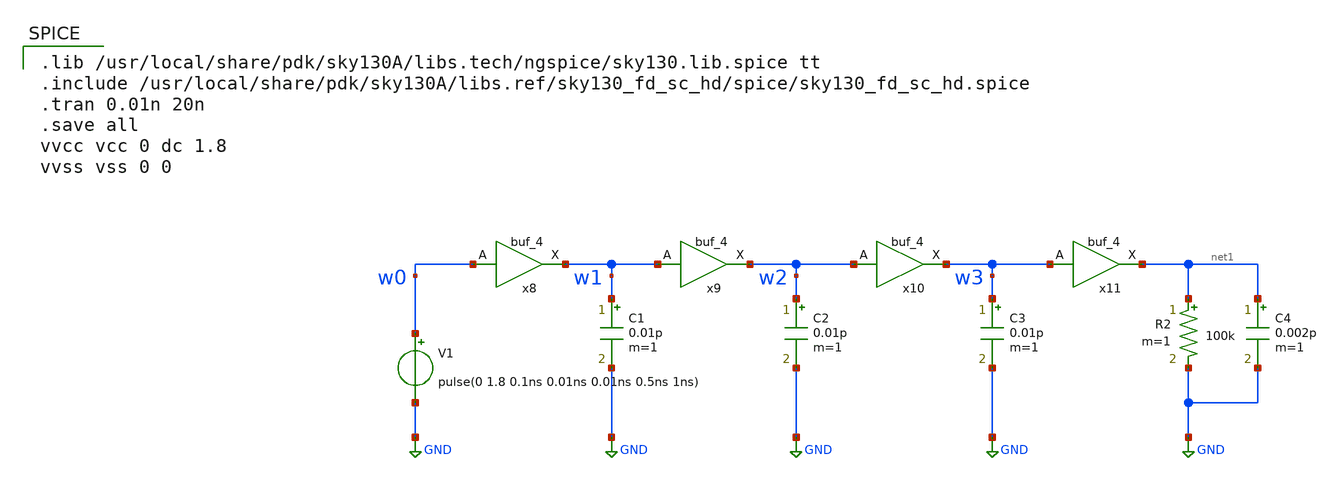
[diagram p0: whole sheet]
** sch_path: sky130-sim/buffer_chain/buffer_chain.sch
**.subckt buffer_chain
x8 w0 VGND VNB VPB VPWR w1 sky130_fd_sc_hd__buf_4
C1 w1 GND 0.01p m=1
x9 w1 VGND VNB VPB VPWR w2 sky130_fd_sc_hd__buf_4
C2 w2 GND 0.01p m=1
x10 w2 VGND VNB VPB VPWR w3 sky130_fd_sc_hd__buf_4
C3 w3 GND 0.01p m=1
x11 w3 VGND VNB VPB VPWR net1 sky130_fd_sc_hd__buf_4
R2 net1 GND 100k m=1
C4 net1 GND 0.002p m=1
V1 w0 GND pulse(0 1.8 0.1ns 0.01ns 0.01ns 0.5ns 1ns)
**** begin user architecture code

.lib /usr/local/share/pdk/sky130A/libs.tech/ngspice/sky130.lib.spice tt
.include /usr/local/share/pdk/sky130A/libs.ref/sky130_fd_sc_hd/spice/sky130_fd_sc_hd.spice
.tran 0.01n 20n
.save all
vvcc vcc 0 dc 1.8
vvss vss 0 0


**** end user architecture code
**.ends
.GLOBAL GND
.end
